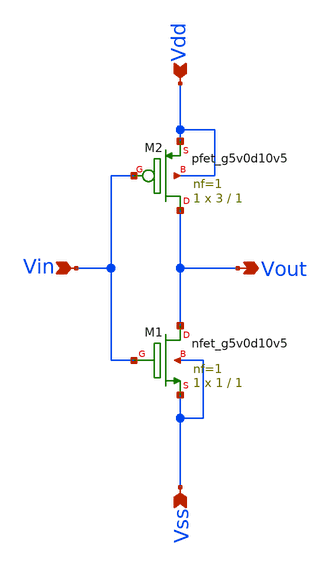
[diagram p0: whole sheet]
** sch_path: xschem/NOT_GATE.sch
**.subckt NOT_GATE Vout Vdd Vss Vin
*.opin Vout
*.ipin Vdd
*.ipin Vss
*.ipin Vin
XM1 Vout Vin Vss Vss sky130_fd_pr__nfet_g5v0d10v5 L=1 W=1 nf=1 ad='int((1 + 1)/2) * 1 / 1 * 0.29' as='int((1 + 2)/2) * 1 / 1 * 0.29'
+ pd='2*int((1 + 1)/2) * (1 / 1 + 0.29)' ps='2*int((1 + 2)/2) * (1 / 1 + 0.29)' nrd='0.29 / 1 ' nrs='0.29 / 1 '
+ sa=0 sb=0 sd=0 mult=1 m=1
XM2 Vout Vin Vdd Vdd sky130_fd_pr__pfet_g5v0d10v5 L=1 W=3 nf=1 ad='int((1 + 1)/2) * 3 / 1 * 0.29' as='int((1 + 2)/2) * 3 / 1 * 0.29'
+ pd='2*int((1 + 1)/2) * (3 / 1 + 0.29)' ps='2*int((1 + 2)/2) * (3 / 1 + 0.29)' nrd='0.29 / 3 ' nrs='0.29 / 3 '
+ sa=0 sb=0 sd=0 mult=1 m=1
**.ends
.end
